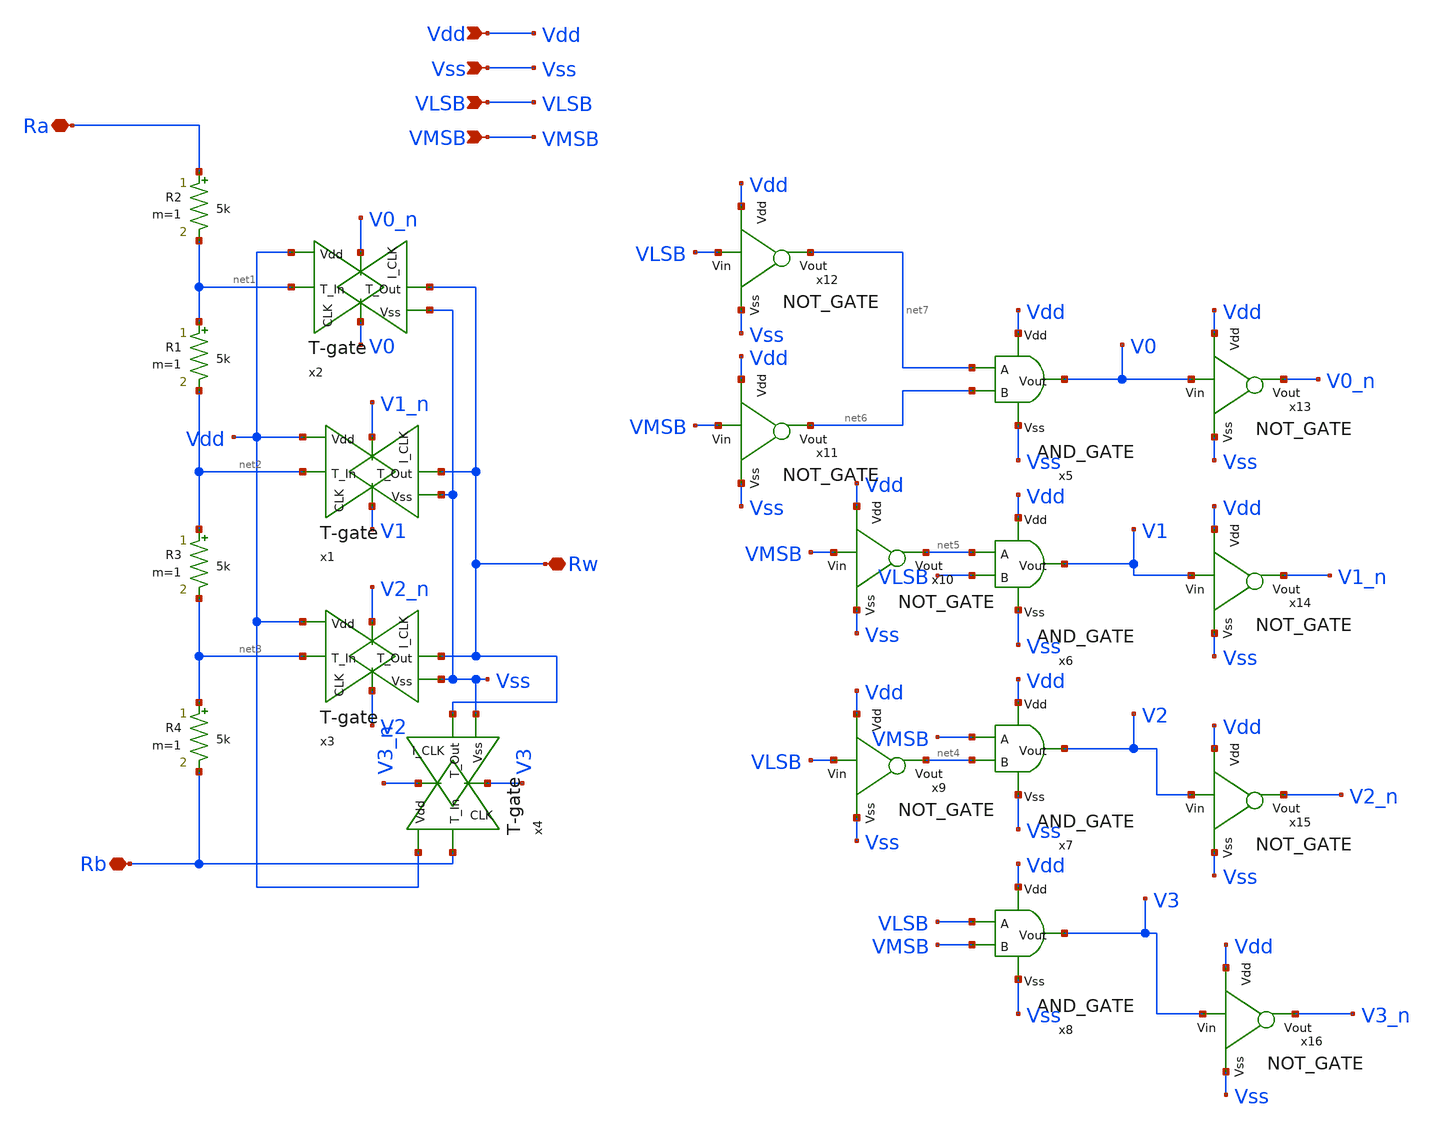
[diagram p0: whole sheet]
** sch_path: xschem/Dig_Pot.sch
**.subckt Dig_Pot Ra Rb Rw Vdd Vss VLSB VMSB
*.iopin Ra
*.iopin Rb
*.iopin Rw
*.ipin Vdd
*.ipin Vss
*.ipin VLSB
*.ipin VMSB
x2 V0_n net1 Rw Vdd Vss V0 T-gate
x1 V1_n net2 Rw Vdd Vss V1 T-gate
x3 V2_n net3 Rw Vdd Vss V2 T-gate
R2 Ra net1 5k m=1
R1 net1 net2 5k m=1
R3 net2 net3 5k m=1
x4 V3_n Rb Rw Vdd Vss V3 T-gate
R4 net3 Rb 5k m=1
x5 Vdd net7 net6 V0 Vss AND_GATE
x6 Vdd net5 VLSB V1 Vss AND_GATE
x7 Vdd VMSB net4 V2 Vss AND_GATE
x8 Vdd VLSB VMSB V3 Vss AND_GATE
x9 Vdd net4 VLSB Vss NOT_GATE
x10 Vdd net5 VMSB Vss NOT_GATE
x11 Vdd net6 VMSB Vss NOT_GATE
x12 Vdd net7 VLSB Vss NOT_GATE
x13 Vdd V0_n V0 Vss NOT_GATE
x14 Vdd V1_n V1 Vss NOT_GATE
x15 Vdd V2_n V2 Vss NOT_GATE
x16 Vdd V3_n V3 Vss NOT_GATE
**.ends
.end
